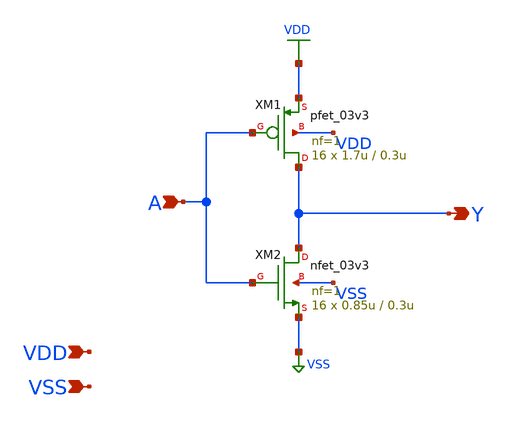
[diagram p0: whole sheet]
** sch_path: gf180mcu_osu_sc_gp12t3v3/xschem/gf180mcu_osu_sc_gp12t3v3__clkinv_16.sch
**.subckt gf180mcu_osu_sc_gp12t3v3__clkinv_16 A Y VDD VSS
*.ipin A
*.opin Y
*.ipin VDD
*.ipin VSS
XM1 Y A VDD VDD pfet_03v3 L=0.3u W=1.7u nf=1 ad='int((nf+1)/2) * W/nf * 0.18u' as='int((nf+2)/2) * W/nf * 0.18u'
+ pd='2*int((nf+1)/2) * (W/nf + 0.18u)' ps='2*int((nf+2)/2) * (W/nf + 0.18u)' nrd='0.18u / W' nrs='0.18u / W'
+ sa=0 sb=0 sd=0 m=16
XM2 Y A VSS VSS nfet_03v3 L=0.3u W=0.85u nf=1 ad='int((nf+1)/2) * W/nf * 0.18u' as='int((nf+2)/2) * W/nf * 0.18u'
+ pd='2*int((nf+1)/2) * (W/nf + 0.18u)' ps='2*int((nf+2)/2) * (W/nf + 0.18u)' nrd='0.18u / W' nrs='0.18u / W'
+ sa=0 sb=0 sd=0 m=16
**.ends
.GLOBAL VDD
.GLOBAL VSS
.end
